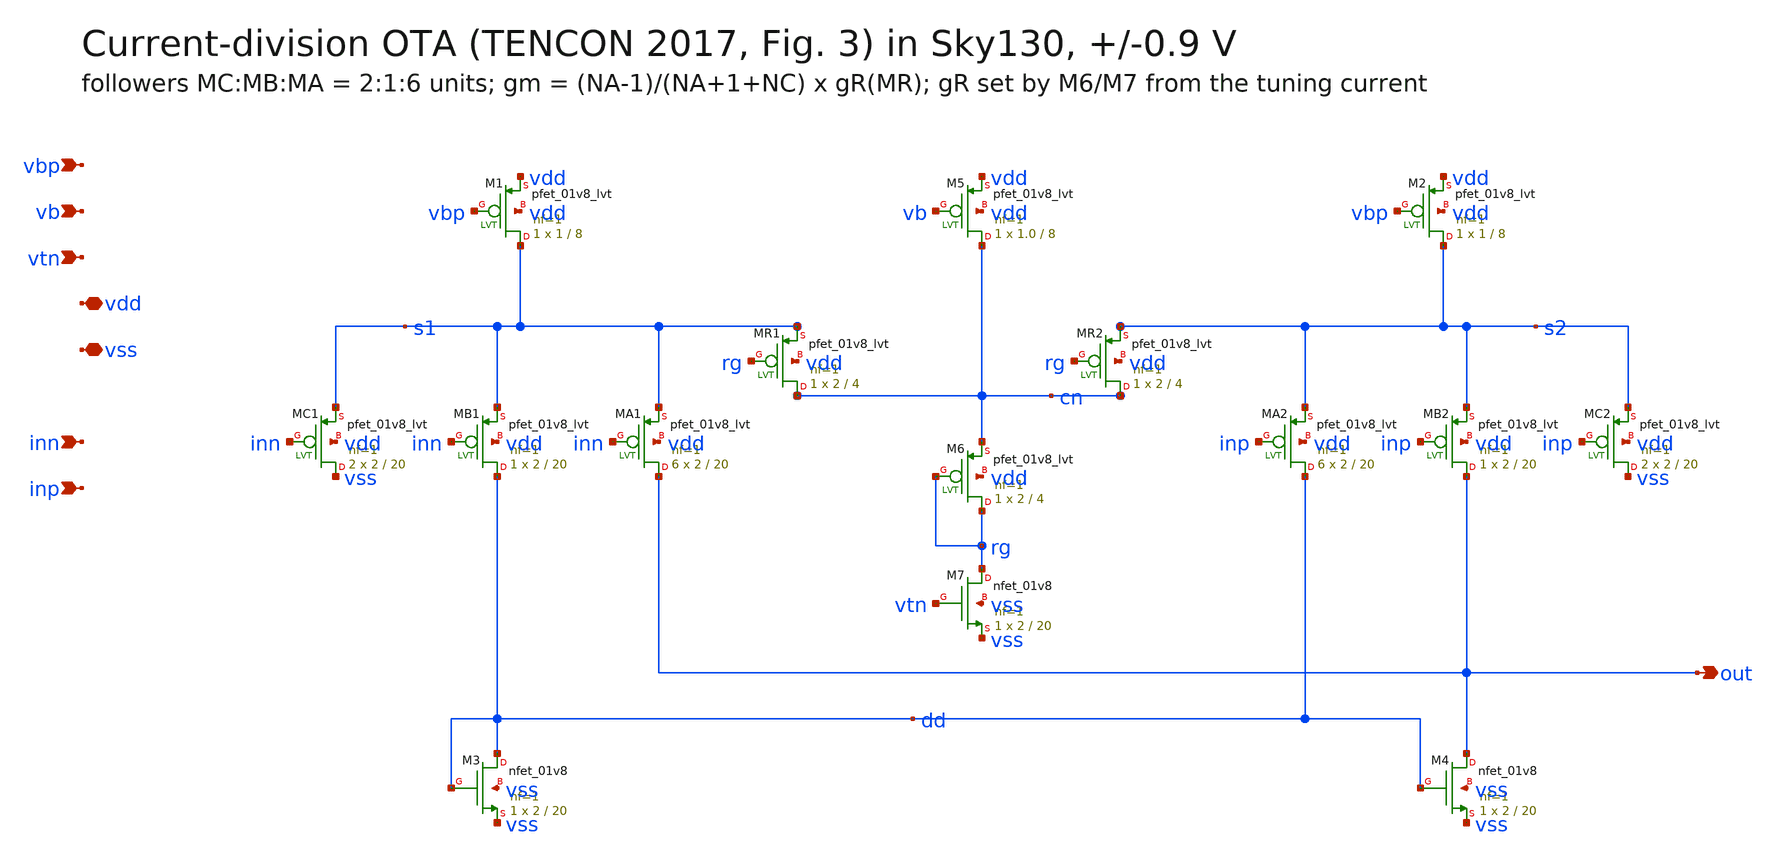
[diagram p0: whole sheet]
** sch_path: notch_ota_current_division/schematics/ota_cd.sch
**.subckt ota_cd inn inp out vbp vb vtn vdd vss
*.ipin inn
*.ipin inp
*.opin out
*.ipin vbp
*.ipin vb
*.ipin vtn
*.iopin vdd
*.iopin vss
XM1 s1 vbp vdd vdd sky130_fd_pr__pfet_01v8_lvt L=8 W=1 nf=1 ad='int((nf+1)/2) * W/nf * 0.29' as='int((nf+2)/2) * W/nf * 0.29'
+ pd='2*int((nf+1)/2) * (W/nf + 0.29)' ps='2*int((nf+2)/2) * (W/nf + 0.29)' nrd='0.29 / W' nrs='0.29 / W'
+ sa=0 sb=0 sd=0 mult=1 m=1
XM5 cn vb vdd vdd sky130_fd_pr__pfet_01v8_lvt L=8 W=1.0 nf=1 ad='int((nf+1)/2) * W/nf * 0.29' as='int((nf+2)/2) * W/nf * 0.29'
+ pd='2*int((nf+1)/2) * (W/nf + 0.29)' ps='2*int((nf+2)/2) * (W/nf + 0.29)' nrd='0.29 / W' nrs='0.29 / W'
+ sa=0 sb=0 sd=0 mult=1 m=1
XM2 s2 vbp vdd vdd sky130_fd_pr__pfet_01v8_lvt L=8 W=1 nf=1 ad='int((nf+1)/2) * W/nf * 0.29' as='int((nf+2)/2) * W/nf * 0.29'
+ pd='2*int((nf+1)/2) * (W/nf + 0.29)' ps='2*int((nf+2)/2) * (W/nf + 0.29)' nrd='0.29 / W' nrs='0.29 / W'
+ sa=0 sb=0 sd=0 mult=1 m=1
XMC1 vss inn s1 vdd sky130_fd_pr__pfet_01v8_lvt L=20 W=2 nf=1 ad='int((nf+1)/2) * W/nf * 0.29' as='int((nf+2)/2) * W/nf * 0.29'
+ pd='2*int((nf+1)/2) * (W/nf + 0.29)' ps='2*int((nf+2)/2) * (W/nf + 0.29)' nrd='0.29 / W' nrs='0.29 / W'
+ sa=0 sb=0 sd=0 mult=2 m=2
XMB1 dd inn s1 vdd sky130_fd_pr__pfet_01v8_lvt L=20 W=2 nf=1 ad='int((nf+1)/2) * W/nf * 0.29' as='int((nf+2)/2) * W/nf * 0.29'
+ pd='2*int((nf+1)/2) * (W/nf + 0.29)' ps='2*int((nf+2)/2) * (W/nf + 0.29)' nrd='0.29 / W' nrs='0.29 / W'
+ sa=0 sb=0 sd=0 mult=1 m=1
XMA1 out inn s1 vdd sky130_fd_pr__pfet_01v8_lvt L=20 W=2 nf=1 ad='int((nf+1)/2) * W/nf * 0.29' as='int((nf+2)/2) * W/nf * 0.29'
+ pd='2*int((nf+1)/2) * (W/nf + 0.29)' ps='2*int((nf+2)/2) * (W/nf + 0.29)' nrd='0.29 / W' nrs='0.29 / W'
+ sa=0 sb=0 sd=0 mult=6 m=6
XMA2 dd inp s2 vdd sky130_fd_pr__pfet_01v8_lvt L=20 W=2 nf=1 ad='int((nf+1)/2) * W/nf * 0.29' as='int((nf+2)/2) * W/nf * 0.29'
+ pd='2*int((nf+1)/2) * (W/nf + 0.29)' ps='2*int((nf+2)/2) * (W/nf + 0.29)' nrd='0.29 / W' nrs='0.29 / W'
+ sa=0 sb=0 sd=0 mult=6 m=6
XMB2 out inp s2 vdd sky130_fd_pr__pfet_01v8_lvt L=20 W=2 nf=1 ad='int((nf+1)/2) * W/nf * 0.29' as='int((nf+2)/2) * W/nf * 0.29'
+ pd='2*int((nf+1)/2) * (W/nf + 0.29)' ps='2*int((nf+2)/2) * (W/nf + 0.29)' nrd='0.29 / W' nrs='0.29 / W'
+ sa=0 sb=0 sd=0 mult=1 m=1
XMC2 vss inp s2 vdd sky130_fd_pr__pfet_01v8_lvt L=20 W=2 nf=1 ad='int((nf+1)/2) * W/nf * 0.29' as='int((nf+2)/2) * W/nf * 0.29'
+ pd='2*int((nf+1)/2) * (W/nf + 0.29)' ps='2*int((nf+2)/2) * (W/nf + 0.29)' nrd='0.29 / W' nrs='0.29 / W'
+ sa=0 sb=0 sd=0 mult=2 m=2
XMR1 cn rg s1 vdd sky130_fd_pr__pfet_01v8_lvt L=4 W=2 nf=1 ad='int((nf+1)/2) * W/nf * 0.29' as='int((nf+2)/2) * W/nf * 0.29'
+ pd='2*int((nf+1)/2) * (W/nf + 0.29)' ps='2*int((nf+2)/2) * (W/nf + 0.29)' nrd='0.29 / W' nrs='0.29 / W'
+ sa=0 sb=0 sd=0 mult=1 m=1
XMR2 cn rg s2 vdd sky130_fd_pr__pfet_01v8_lvt L=4 W=2 nf=1 ad='int((nf+1)/2) * W/nf * 0.29' as='int((nf+2)/2) * W/nf * 0.29'
+ pd='2*int((nf+1)/2) * (W/nf + 0.29)' ps='2*int((nf+2)/2) * (W/nf + 0.29)' nrd='0.29 / W' nrs='0.29 / W'
+ sa=0 sb=0 sd=0 mult=1 m=1
XM6 rg rg cn vdd sky130_fd_pr__pfet_01v8_lvt L=4 W=2 nf=1 ad='int((nf+1)/2) * W/nf * 0.29' as='int((nf+2)/2) * W/nf * 0.29'
+ pd='2*int((nf+1)/2) * (W/nf + 0.29)' ps='2*int((nf+2)/2) * (W/nf + 0.29)' nrd='0.29 / W' nrs='0.29 / W'
+ sa=0 sb=0 sd=0 mult=1 m=1
XM7 rg vtn vss vss sky130_fd_pr__nfet_01v8 L=20 W=2 nf=1 ad='int((nf+1)/2) * W/nf * 0.29' as='int((nf+2)/2) * W/nf * 0.29'
+ pd='2*int((nf+1)/2) * (W/nf + 0.29)' ps='2*int((nf+2)/2) * (W/nf + 0.29)' nrd='0.29 / W' nrs='0.29 / W'
+ sa=0 sb=0 sd=0 mult=1 m=1
XM3 dd dd vss vss sky130_fd_pr__nfet_01v8 L=20 W=2 nf=1 ad='int((nf+1)/2) * W/nf * 0.29' as='int((nf+2)/2) * W/nf * 0.29'
+ pd='2*int((nf+1)/2) * (W/nf + 0.29)' ps='2*int((nf+2)/2) * (W/nf + 0.29)' nrd='0.29 / W' nrs='0.29 / W'
+ sa=0 sb=0 sd=0 mult=1 m=1
XM4 out dd vss vss sky130_fd_pr__nfet_01v8 L=20 W=2 nf=1 ad='int((nf+1)/2) * W/nf * 0.29' as='int((nf+2)/2) * W/nf * 0.29'
+ pd='2*int((nf+1)/2) * (W/nf + 0.29)' ps='2*int((nf+2)/2) * (W/nf + 0.29)' nrd='0.29 / W' nrs='0.29 / W'
+ sa=0 sb=0 sd=0 mult=1 m=1
**.ends
.end
